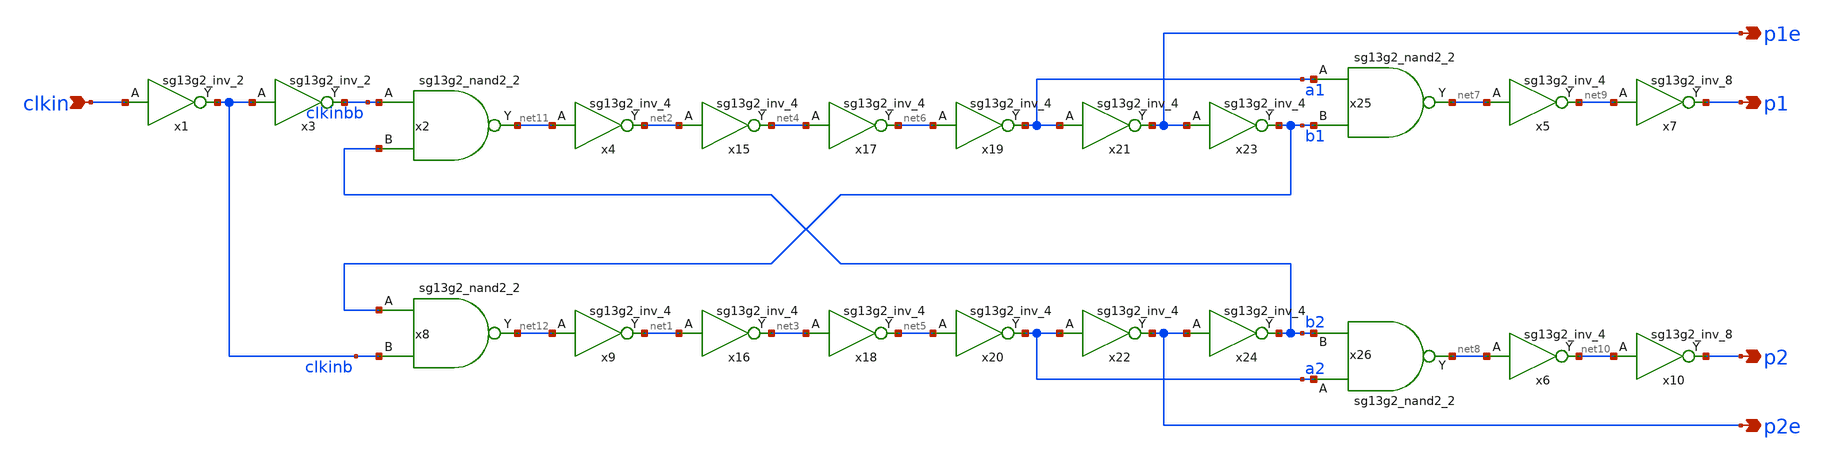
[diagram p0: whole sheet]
** sch_path: 5_Design/4_Layout/Team 1/xschem/clk_generator_t1.sch
* IHP-GmbH/IHP-Open-PDK/ihp-sg13g2/libs.tech/xschem/sg13g2_stdcells/sg13g2_inv_2.sch:
* Copyright 2023 IHP PDK Authors
* Licensed under the Apache License, Version 2.0 (the "License");
**.subckt clk_generator_t1 clkin p2e p2 p1 p1e
*.ipin clkin
*.opin p2e
*.opin p2
*.opin p1
*.opin p1e
x1 clkinb clkin VDD VSS sg13g2_inv_2
x2 net11 clkinbb b2 VDD VSS sg13g2_nand2_2
x3 clkinbb clkinb VDD VSS sg13g2_inv_2
x4 net2 net11 VDD VSS sg13g2_inv_4
x8 net12 b1 clkinb VDD VSS sg13g2_nand2_2
x9 net1 net12 VDD VSS sg13g2_inv_4
x15 net4 net2 VDD VSS sg13g2_inv_4
x16 net3 net1 VDD VSS sg13g2_inv_4
x17 net6 net4 VDD VSS sg13g2_inv_4
x18 net5 net3 VDD VSS sg13g2_inv_4
x19 a1 net6 VDD VSS sg13g2_inv_4
x20 a2 net5 VDD VSS sg13g2_inv_4
x21 p1e a1 VDD VSS sg13g2_inv_4
x22 p2e a2 VDD VSS sg13g2_inv_4
x23 b1 p1e VDD VSS sg13g2_inv_4
x24 b2 p2e VDD VSS sg13g2_inv_4
x25 net7 a1 b1 VDD VSS sg13g2_nand2_2
x26 net8 a2 b2 VDD VSS sg13g2_nand2_2
x5 net9 net7 VDD VSS sg13g2_inv_4
x6 net10 net8 VDD VSS sg13g2_inv_4
x7 p1 net9 VDD VSS sg13g2_inv_8
x10 p2 net10 VDD VSS sg13g2_inv_8
**.ends

* expanding   symbol:  sg13g2_stdcells/sg13g2_inv_2.sym # of pins=2
** sym_path: sg13g2_stdcells/sg13g2_inv_2.sym
** sch_path: sg13g2_stdcells/sg13g2_inv_2.sch
.subckt sg13g2_inv_2 Y A VDD VSS
*.opin Y
*.ipin A
*.iopin VDD
*.iopin VSS
XM1 Y A VSS VSS sg13_lv_nmos w=1.48u l=130.00n ng=2 m=1 mm_ok=1
XM2 Y A VDD VDD sg13_lv_pmos w=2.24u l=130.00n ng=2 m=1 mm_ok=1
.ends


* expanding   symbol:  sg13g2_stdcells/sg13g2_nand2_2.sym # of pins=3
** sym_path: sg13g2_stdcells/sg13g2_nand2_2.sym
** sch_path: sg13g2_stdcells/sg13g2_nand2_2.sch
.subckt sg13g2_nand2_2 Y A B VDD VSS
*.iopin VDD
*.iopin VSS
*.opin Y
*.ipin B
*.ipin A
XM1 Y A net1 VSS sg13_lv_nmos w=1.44u l=130.00n ng=2 m=1 mm_ok=1
XM2 net1 B VSS VSS sg13_lv_nmos w=1.44u l=130.00n ng=2 m=1 mm_ok=1
XM3 Y A VDD VDD sg13_lv_pmos w=2.24u l=130.00n ng=2 m=1 mm_ok=1
XM4 Y B VDD VDD sg13_lv_pmos w=2.24u l=130.00n ng=2 m=1 mm_ok=1
.ends


* expanding   symbol:  sg13g2_stdcells/sg13g2_inv_4.sym # of pins=2
** sym_path: sg13g2_stdcells/sg13g2_inv_4.sym
** sch_path: sg13g2_stdcells/sg13g2_inv_4.sch
.subckt sg13g2_inv_4 Y A VDD VSS
*.ipin A
*.opin Y
*.iopin VDD
*.iopin VSS
XM1 Y A VSS VSS sg13_lv_nmos w=2.96u l=130.00n ng=4 m=1 mm_ok=1
XM2 Y A VDD VDD sg13_lv_pmos w=4.48u l=130.00n ng=4 m=1 mm_ok=1
.ends


* expanding   symbol:  sg13g2_stdcells/sg13g2_inv_8.sym # of pins=2
** sym_path: sg13g2_stdcells/sg13g2_inv_8.sym
** sch_path: sg13g2_stdcells/sg13g2_inv_8.sch
.subckt sg13g2_inv_8 Y A VDD VSS
*.opin Y
*.ipin A
*.iopin VDD
*.iopin VSS
XM1 Y A VSS VSS sg13_lv_nmos w=5.92u l=130.00n ng=8 m=1 mm_ok=1
XM2 Y A VDD VDD sg13_lv_pmos w=8.96u l=130.00n ng=8 m=1 mm_ok=1
.ends

.end
